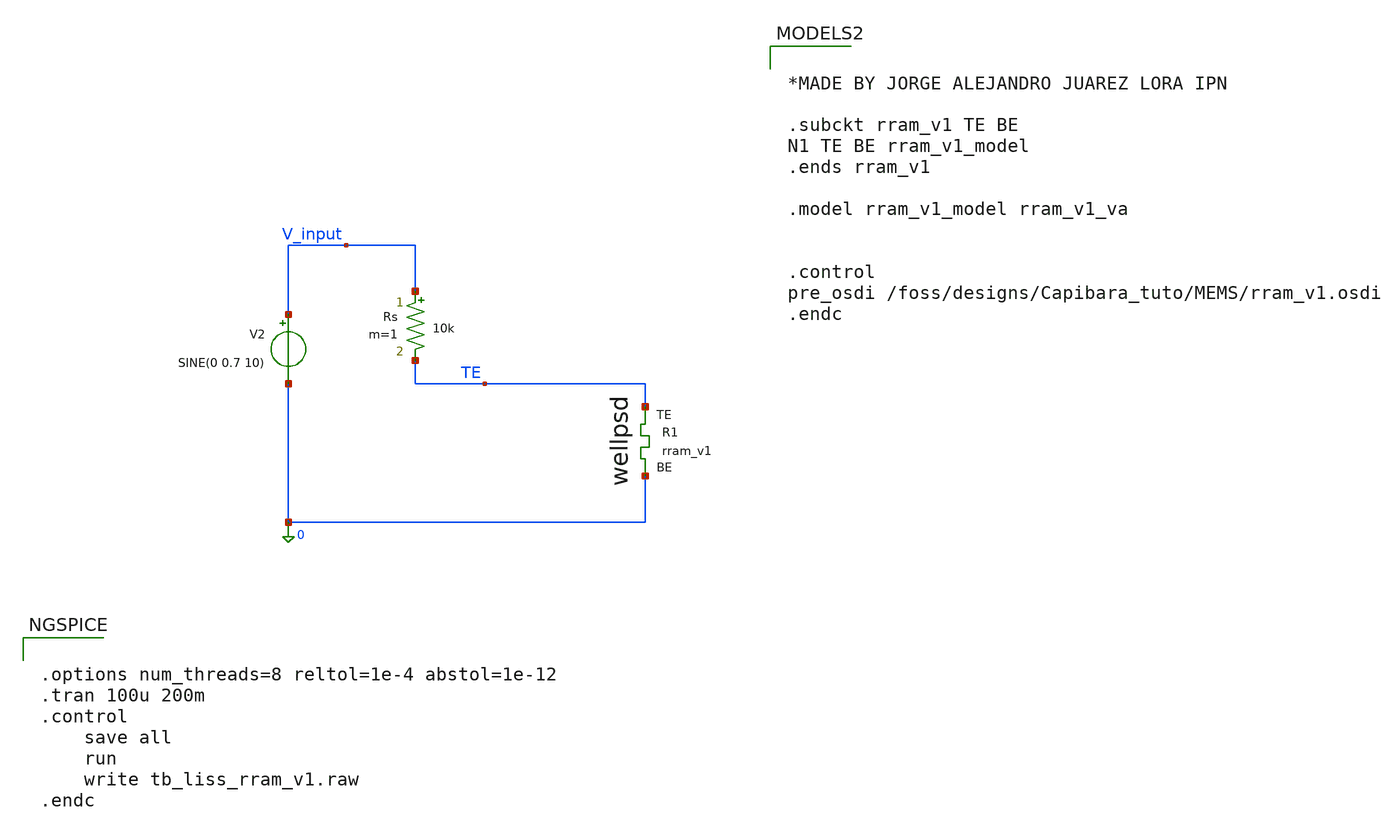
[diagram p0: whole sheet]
** sch_path: tb_liss_rram_v1_with_Rs.sch
**.subckt tb_liss_rram_v1_with_Rs
V2 V_input 0 SINE(0 0.7 10)
XR1 TE 0 rram_v1
Rs V_input TE 10k m=1
**** begin user architecture code


.options num_threads=8 reltol=1e-4 abstol=1e-12
.tran 100u 200m
.control
	save all
	run
	write tb_liss_rram_v1.raw
.endc




*MADE BY JORGE ALEJANDRO JUAREZ LORA IPN

.subckt rram_v1 TE BE
N1 TE BE rram_v1_model
.ends rram_v1

.model rram_v1_model rram_v1_va


.control
pre_osdi /foss/designs/Capibara_tuto/MEMS/rram_v1.osdi
.endc

**** end user architecture code
**.ends
.end
